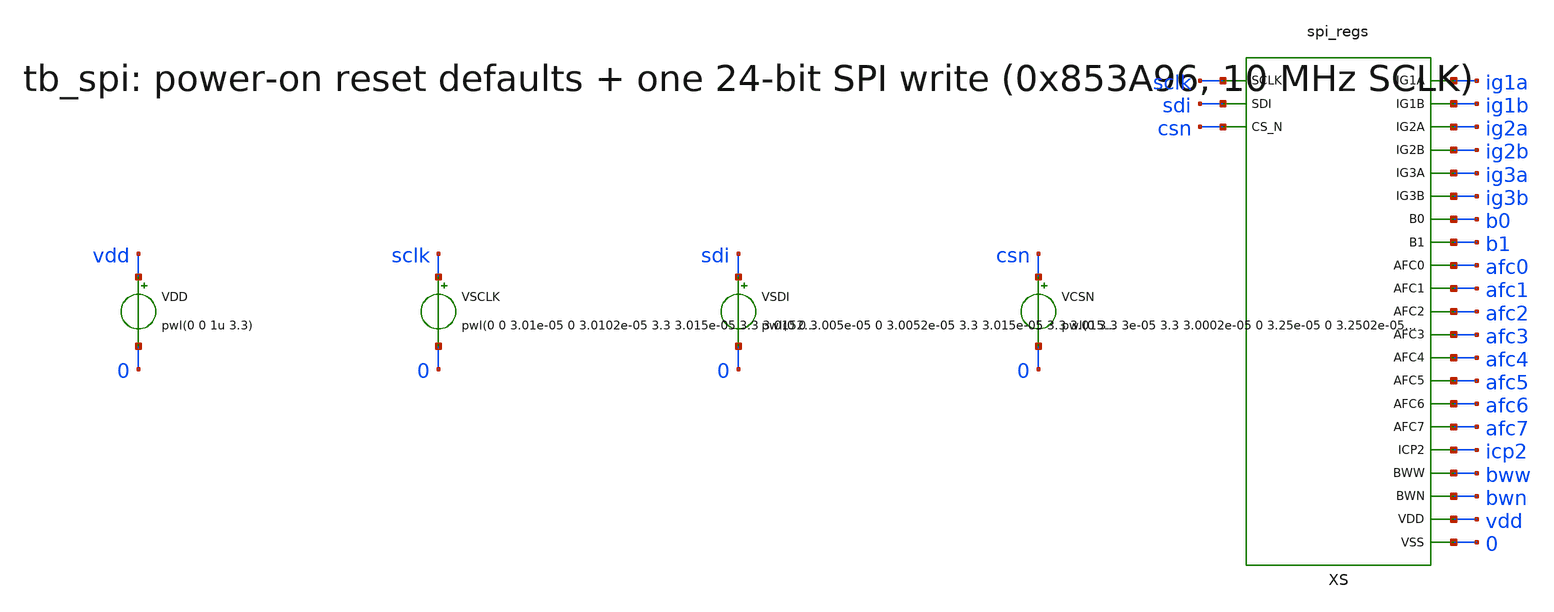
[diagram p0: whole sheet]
** sch_path: v1_claude/xschem/tb_spi.sch
**.subckt tb_spi
VDD vdd 0 pwl(0 0 1u 3.3)
VSCLK sclk 0 pwl(0 0 3.01e-05 0 3.0102e-05 3.3 3.015e-05 3.3 3.0152e-05 0 3.02e-05 0 3.0202e-05 3.3
+ 3.025e-05 3.3 3.0252e-05 0 3.03e-05 0 3.0302e-05 3.3 3.035e-05 3.3 3.0352e-05 0 3.04e-05 0 3.0402e-05 3.3
+ 3.045e-05 3.3 3.0452e-05 0 3.05e-05 0 3.0502e-05 3.3 3.055e-05 3.3 3.0552e-05 0 3.06e-05 0 3.0602e-05 3.3
+ 3.065e-05 3.3 3.0652e-05 0 3.07e-05 0 3.0702e-05 3.3 3.075e-05 3.3 3.0752e-05 0 3.08e-05 0 3.0802e-05 3.3
+ 3.085e-05 3.3 3.0852e-05 0 3.09e-05 0 3.0902e-05 3.3 3.095e-05 3.3 3.0952e-05 0 3.1e-05 0 3.1002e-05 3.3
+ 3.105e-05 3.3 3.1052e-05 0 3.11e-05 0 3.1102e-05 3.3 3.115e-05 3.3 3.1152e-05 0 3.12e-05 0 3.1202e-05 3.3
+ 3.125e-05 3.3 3.1252e-05 0 3.13e-05 0 3.1302e-05 3.3 3.135e-05 3.3 3.1352e-05 0 3.14e-05 0 3.1402e-05 3.3
+ 3.145e-05 3.3 3.1452e-05 0 3.15e-05 0 3.1502e-05 3.3 3.155e-05 3.3 3.1552e-05 0 3.16e-05 0 3.1602e-05 3.3
+ 3.165e-05 3.3 3.1652e-05 0 3.17e-05 0 3.1702e-05 3.3 3.175e-05 3.3 3.1752e-05 0 3.18e-05 0 3.1802e-05 3.3
+ 3.185e-05 3.3 3.1852e-05 0 3.19e-05 0 3.1902e-05 3.3 3.195e-05 3.3 3.1952e-05 0 3.2e-05 0 3.2002e-05 3.3
+ 3.205e-05 3.3 3.2052e-05 0 3.21e-05 0 3.2102e-05 3.3 3.215e-05 3.3 3.2152e-05 0 3.22e-05 0 3.2202e-05 3.3
+ 3.225e-05 3.3 3.2252e-05 0 3.23e-05 0 3.2302e-05 3.3 3.235e-05 3.3 3.2352e-05 0 3.24e-05 0 3.2402e-05 3.3
+ 3.245e-05 3.3 3.2452e-05 0)
VSDI sdi 0 pwl(0 0 3.005e-05 0 3.0052e-05 3.3 3.015e-05 3.3 3.0152e-05 0 3.025e-05 0 3.0252e-05 0
+ 3.035e-05 0 3.0352e-05 0 3.045e-05 0 3.0452e-05 0 3.055e-05 0 3.0552e-05 3.3 3.065e-05 3.3 3.0652e-05 0
+ 3.075e-05 0 3.0752e-05 3.3 3.085e-05 3.3 3.0852e-05 0 3.095e-05 0 3.0952e-05 0 3.105e-05 0 3.1052e-05 3.3
+ 3.115e-05 3.3 3.1152e-05 3.3 3.125e-05 3.3 3.1252e-05 3.3 3.135e-05 3.3 3.1352e-05 0 3.145e-05 0 3.1452e-05
+ 3.3 3.155e-05 3.3 3.1552e-05 0 3.165e-05 0 3.1652e-05 3.3 3.175e-05 3.3 3.1752e-05 0 3.185e-05 0
+ 3.1852e-05 0 3.195e-05 0 3.1952e-05 3.3 3.205e-05 3.3 3.2052e-05 0 3.215e-05 0 3.2152e-05 3.3 3.225e-05 3.3
+ 3.2252e-05 3.3 3.235e-05 3.3 3.2352e-05 0)
VCSN csn 0 pwl(0 3.3 3e-05 3.3 3.0002e-05 0 3.25e-05 0 3.2502e-05 3.3)
XS sclk sdi csn ig1a ig1b ig2a ig2b ig3a ig3b b0 b1 afc0 afc1 afc2 afc3 afc4 afc5 afc6 afc7 icp2 bww
+ bwn vdd 0 spi_regs
**** begin user architecture code
 .include $::180MCU_MODELS/design.ngspice
.lib $::180MCU_MODELS/sm141064.ngspice typical
.lib $::180MCU_MODELS/sm141064.ngspice res_typical
.lib $::180MCU_MODELS/sm141064.ngspice mimcap_typical

.control
set num_threads=1
tran 2n 34.5u
meas tran por_ig1a find v(ig1a) at=2.9e-05
meas tran por_ig1b find v(ig1b) at=2.9e-05
meas tran por_ig2a find v(ig2a) at=2.9e-05
meas tran por_ig2b find v(ig2b) at=2.9e-05
meas tran por_ig3a find v(ig3a) at=2.9e-05
meas tran por_ig3b find v(ig3b) at=2.9e-05
meas tran por_b0 find v(b0) at=2.9e-05
meas tran por_b1 find v(b1) at=2.9e-05
meas tran por_afc0 find v(afc0) at=2.9e-05
meas tran por_afc1 find v(afc1) at=2.9e-05
meas tran por_afc2 find v(afc2) at=2.9e-05
meas tran por_afc3 find v(afc3) at=2.9e-05
meas tran por_afc4 find v(afc4) at=2.9e-05
meas tran por_afc5 find v(afc5) at=2.9e-05
meas tran por_afc6 find v(afc6) at=2.9e-05
meas tran por_afc7 find v(afc7) at=2.9e-05
meas tran por_icp2 find v(icp2) at=2.9e-05
meas tran por_bww find v(bww) at=2.9e-05
meas tran por_bwn find v(bwn) at=2.9e-05
echo RES por IG1A=$&por_ig1a IG1B=$&por_ig1b IG2A=$&por_ig2a IG2B=$&por_ig2b IG3A=$&por_ig3a
+ IG3B=$&por_ig3b B0=$&por_b0 B1=$&por_b1 AFC0=$&por_afc0 AFC1=$&por_afc1 AFC2=$&por_afc2 AFC3=$&por_afc3
+ AFC4=$&por_afc4 AFC5=$&por_afc5 AFC6=$&por_afc6 AFC7=$&por_afc7 ICP2=$&por_icp2 BWW=$&por_bww BWN=$&por_bwn
meas tran write_ig1a find v(ig1a) at=3.4e-05
meas tran write_ig1b find v(ig1b) at=3.4e-05
meas tran write_ig2a find v(ig2a) at=3.4e-05
meas tran write_ig2b find v(ig2b) at=3.4e-05
meas tran write_ig3a find v(ig3a) at=3.4e-05
meas tran write_ig3b find v(ig3b) at=3.4e-05
meas tran write_b0 find v(b0) at=3.4e-05
meas tran write_b1 find v(b1) at=3.4e-05
meas tran write_afc0 find v(afc0) at=3.4e-05
meas tran write_afc1 find v(afc1) at=3.4e-05
meas tran write_afc2 find v(afc2) at=3.4e-05
meas tran write_afc3 find v(afc3) at=3.4e-05
meas tran write_afc4 find v(afc4) at=3.4e-05
meas tran write_afc5 find v(afc5) at=3.4e-05
meas tran write_afc6 find v(afc6) at=3.4e-05
meas tran write_afc7 find v(afc7) at=3.4e-05
meas tran write_icp2 find v(icp2) at=3.4e-05
meas tran write_bww find v(bww) at=3.4e-05
meas tran write_bwn find v(bwn) at=3.4e-05
echo RES write IG1A=$&write_ig1a IG1B=$&write_ig1b IG2A=$&write_ig2a IG2B=$&write_ig2b
+ IG3A=$&write_ig3a IG3B=$&write_ig3b B0=$&write_b0 B1=$&write_b1 AFC0=$&write_afc0 AFC1=$&write_afc1 AFC2=$&write_afc2
+ AFC3=$&write_afc3 AFC4=$&write_afc4 AFC5=$&write_afc5 AFC6=$&write_afc6 AFC7=$&write_afc7 ICP2=$&write_icp2
+ BWW=$&write_bww BWN=$&write_bwn
meas tran rstw when v(xs.rst)=1.65 fall=1
echo RES por_release=$&rstw
.endc

**** end user architecture code
**.ends
.end
